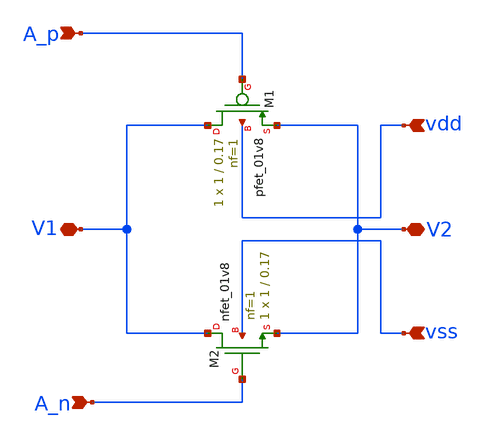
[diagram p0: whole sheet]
** sch_path: xschem/t-gate/t_gate.sch
**.subckt t_gate V1 V2 A_p vdd vss A_n
*.iopin V1
*.iopin V2
*.ipin A_p
*.ipin vdd
*.ipin vss
*.ipin A_n
XM2 V1 A_n V2 vss sky130_fd_pr__nfet_01v8 L=0.17 W=1 nf=1 ad={int((nf+1)/2) * W/nf * 0.29} as={int((nf+2)/2) * W/nf * 0.29}
+ pd={2*int((nf+1)/2) * (W/nf + 0.29)} ps={2*int((nf+2)/2) * (W/nf + 0.29)} nrd={0.29 / W} nrs={0.29 / W}
+ sa=0 sb=0 sd=0 mult=1 m=1
XM1 V1 A_p V2 vdd sky130_fd_pr__pfet_01v8 L=0.17 W=1 nf=1 ad={int((nf+1)/2) * W/nf * 0.29} as={int((nf+2)/2) * W/nf * 0.29}
+ pd={2*int((nf+1)/2) * (W/nf + 0.29)} ps={2*int((nf+2)/2) * (W/nf + 0.29)} nrd={0.29 / W} nrs={0.29 / W}
+ sa=0 sb=0 sd=0 mult=1 m=1
**.ends
.end
